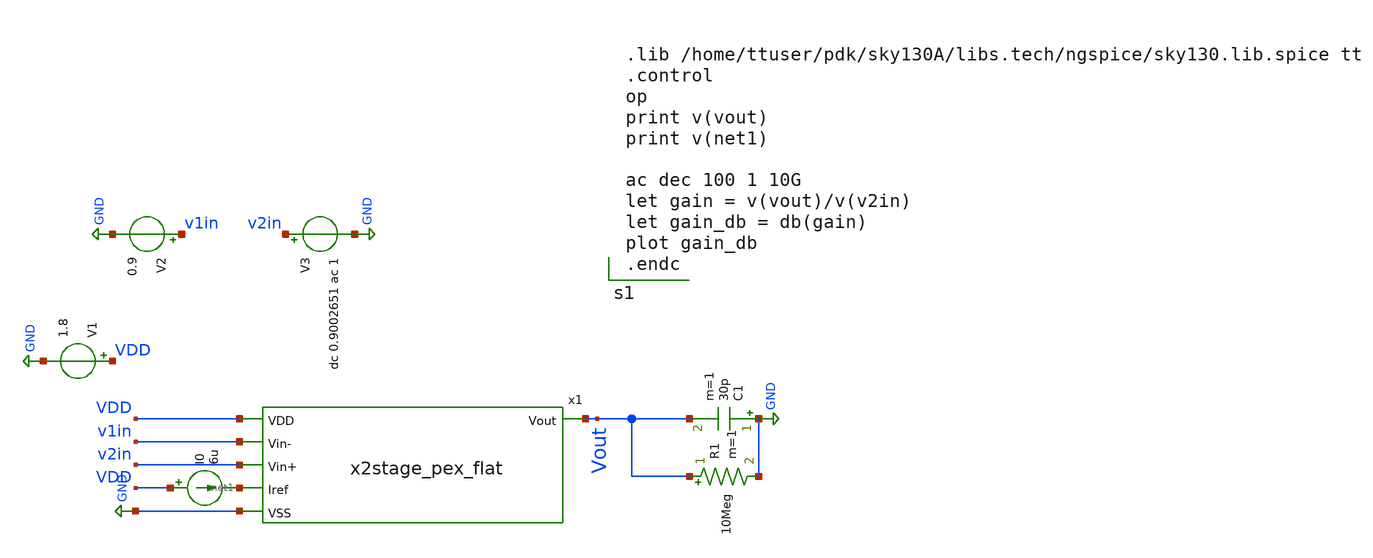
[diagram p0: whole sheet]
** sch_path: testbenches/postlayout/2stage_OL_pexRC.sch
**.subckt 2stage_OL_pexRC
x1 VDD Vout v1in v2in net1 GND x2stage_pex_flat
I0 VDD net1 6u
V1 VDD GND 1.8
V2 v1in GND 0.9
V3 v2in GND dc 0.9002651 ac 1
C1 GND Vout 30p m=1
R1 Vout GND 10Meg m=1
**** begin user architecture code


.lib /home/ttuser/pdk/sky130A/libs.tech/ngspice/sky130.lib.spice tt
.control
op
print v(vout)
print v(net1)

ac dec 100 1 10G
let gain = v(vout)/v(v2in)
let gain_db = db(gain)
plot gain_db
.endc


**** end user architecture code
**.ends

* expanding   symbol:  /home/ttuser/projects/xschem_test/x2stage_pex_flat.sym # of pins=6
** sym_path: schematic/diffpair.sym
.include /home/ttuser/projects/2stage/2stage_pex_flat_c.spice
.GLOBAL GND
.end
